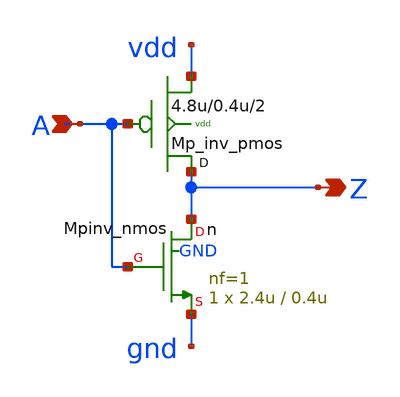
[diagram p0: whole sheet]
** sch_path: sram_4_16_scn4m/pinv_7.sch
**.subckt pinv_7 A Z
*.ipin A
*.opin Z
XMpinv_nmos Z A gnd GND sky130_fd_pr__n L=0.4u W=2.4u nf=1 ad='int((nf+1)/2) * W/nf * 0.29' as='int((nf+2)/2) * W/nf * 0.29'
+ pd='2*int((nf+1)/2) * (W/nf + 0.29)' ps='2*int((nf+2)/2) * (W/nf + 0.29)' nrd='0.29 / W' nrs='0.29 / W'
+ sa=0 sb=0 sd=0 mult=1 m=1
Mp_inv_pmos Z A vdd vdd p w=4.8u l=0.4u m=2
**.ends
.end
